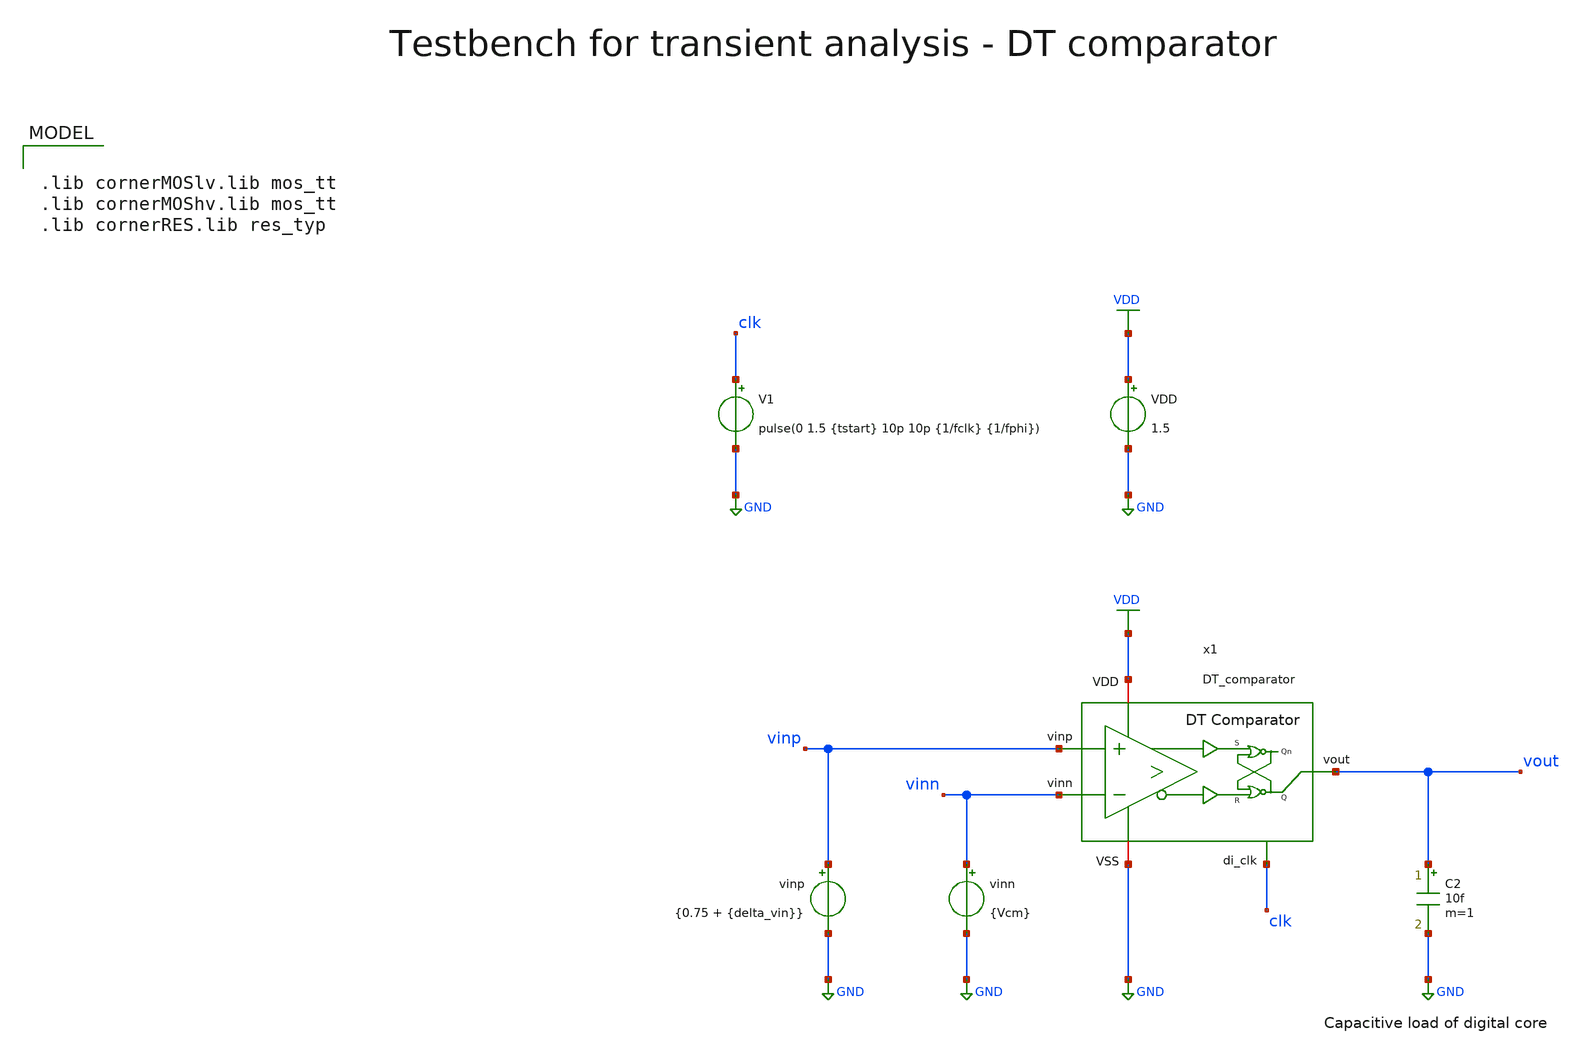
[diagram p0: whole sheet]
** sch_path: SG13G2_ATBS-ADC-main/xschem/comparator/discrete_time/testbenches/DT_comparator_tb_tran.sch
**.subckt DT_comparator_tb_tran
VDD VDD GND 1.5
V1 clk GND pulse(0 1.5 {tstart} 10p 10p {1/fclk} {1/fphi})
vinn vinn GND {Vcm}
vinp vinp GND {0.75 + {delta_vin}}
C2 vout GND 10f m=1
x1 VDD vinp vout vinn clk GND DT_comparator
**** begin user architecture code

.lib cornerMOSlv.lib mos_tt
.lib cornerMOShv.lib mos_tt
.lib cornerRES.lib res_typ



.param temp=27
.param fclk=8000000
.param fphi=62500
.param tstart=2n
.param delta_vin = 10m
.param Vcm=0.75
.csparam fclk=fclk
.csparam tstart=tstart
.options savecurrents reltol=1e-3 abstol=1e-12 gmin=1e-15
.ic v(vout) = 0
.control
save all

* Operating Point Analysis
op
remzerovec
write DT_comparator_tb_tran.raw
set appendwrite

* Transient Analysis
* tran 4p 20n
tran 40p 150n
write DT_comparator_tb_tran.raw

* Measure vcpp_min & vcpn_min
let tmeas = 1/fclk
meas tran vcpp_min FIND v(x1.x1.vcpp) at=tmeas
meas tran vcpn_min FIND v(x1.x1.vcpn) at=tmeas

* Measure Propagation Delay
* Time from clock rising edge to 90% VDD of vout
let vout_limit = 0.9 * 1.5
meas tran tcross WHEN v(vout)=vout_limit CROSS=1
let tpd = tcross - tstart
echo Propagation Delay $&tpd s

* Calculate Energy / Conversion
* i_int in As
* energy_conv in Ws = J
let N = 1
let t_conv = 150n
meas tran i_int INTEG i(VDD) from=tstart to=t_conv
let energy_conv = 1.5 * i_int / N

let energy_conv_femto = energy_conv * 1e15
echo Energy / Conversion $&energy_conv_femto fJ/conv

* Plotting
plot v(clk) v(vinp) v(vinn) v(x1.x1.vs) v(x1.x1.vcpp) v(x1.x1.vcpn) v(x1.voutp_comp)
+ v(x1.voutn_comp) v(vout)
plot i(VDD)

* Writing Data
set wr_singlescale
set wr_vecnames
let vs=x1.x1.vs
let vcpp=x1.x1.vcpp
let vcpn=x1.x1.vcpn
let voutp_comp=x1.voutp_comp
let voutn_comp=x1.voutn_comp
wrdata /foss/designs/SG13G2_ATBS-ADC-main/python/plot_simulations/data/DT_comparator_tb_tran.txt
+ v(clk) v(vinp) v(vinn) v(vs) v(vcpp) v(vcpn) v(voutp_comp) v(voutn_comp) v(vout)

*quit
.endc

**** end user architecture code
**.ends

* expanding   symbol:  comparator/discrete_time/DT_comparator.sym # of pins=6
** sym_path: SG13G2_ATBS-ADC-main/xschem/comparator/discrete_time/DT_comparator.sym
** sch_path: SG13G2_ATBS-ADC-main/xschem/comparator/discrete_time/DT_comparator.sch
.subckt DT_comparator VDD vinp vout vinn di_clk VSS
*.iopin VDD
*.opin vout
*.iopin VSS
*.ipin vinp
*.ipin vinn
*.ipin di_clk
x2 VDD voutp_comp voutp_buf VSS buffer_lv W_P_INV=1.0u L_P_INV=0.13u W_N_INV=1.0u L_N_INV=0.13u
x3 VDD voutn_comp voutn_buf VSS buffer_lv W_P_INV=1.0u L_P_INV=0.13u W_N_INV=1.0u L_N_INV=0.13u
x5 VDD di_clk net1 VSS inverter_lv W_P=1.0u L_P=0.13u W_N=1.0u L_N=0.13u
* noconn #net2
x4 VDD voutp_buf net2 VSS vout voutn_buf SR_latch W_P_SR=1.0u L_P_SR=0.13u W_N_SR=1.0u L_N_SR=0.13u
x1 net1 di_clk VDD voutp_comp vinp VSS voutn_comp vinn dynamic_biasing_comparator
.ends


* expanding   symbol:  buffer/buffer_lv.sym # of pins=4
** sym_path: SG13G2_ATBS-ADC-main/xschem/buffer/buffer_lv.sym
** sch_path: SG13G2_ATBS-ADC-main/xschem/buffer/buffer_lv.sch
.subckt buffer_lv VDD vin vout VSS  W_P_INV=3.0u L_P_INV=0.13u W_N_INV=1.0u L_N_INV=0.13u
*.ipin vin
*.iopin VDD
*.iopin VSS
*.opin vout
x1 VDD vin net1 VSS inverter_lv W_P=W_P_INV L_P=L_P_INV W_N=W_N_INV L_N=L_N_INV
x2 VDD net1 vout VSS inverter_lv W_P=W_P_INV L_P=L_P_INV W_N=W_N_INV L_N=L_N_INV
.ends


* expanding   symbol:  inverter/inverter_lv.sym # of pins=4
** sym_path: SG13G2_ATBS-ADC-main/xschem/inverter/inverter_lv.sym
** sch_path: SG13G2_ATBS-ADC-main/xschem/inverter/inverter_lv.sch
.subckt inverter_lv VDD vin vout VSS  W_P=3.0u L_P=0.13u W_N=1.0u L_N=0.13u
*.ipin vin
*.iopin VDD
*.iopin VSS
*.opin vout
XM1 vout vin VDD VDD sg13_lv_pmos w=W_P l=L_P ng=1 m=1 mm_ok=1
XM2 vout vin VSS VSS sg13_lv_nmos w=W_N l=L_N ng=1 m=1 mm_ok=1
.ends


* expanding   symbol:  comparator/SR_latch/SR_latch.sym # of pins=6
** sym_path: SG13G2_ATBS-ADC-main/xschem/comparator/SR_latch/SR_latch.sym
** sch_path: SG13G2_ATBS-ADC-main/xschem/comparator/SR_latch/SR_latch.sch
.subckt SR_latch VDD S Qn VSS Q R  W_P_SR=1.0u L_P_SR=0.13u W_N_SR=1.0u L_N_SR=0.13u
*.iopin VDD
*.opin Q
*.iopin VSS
*.ipin S
*.ipin R
*.opin Qn
x1 VDD Q R Qn VSS NOR_gate W_P=W_P_SR L_P=L_P_SR W_N=W_N_SR L_N=L_N_SR
x2 VDD Qn Q S VSS NOR_gate W_P=W_P_SR L_P=L_P_SR W_N=W_N_SR L_N=L_N_SR
.ends


* expanding   symbol:  comparator/discrete_time/Dynamic-biasing/dynamic_biasing_comparator.sym # of
*+ pins=8
** sym_path: SG13G2_ATBS-ADC-main/xschem/comparator/discrete_time/Dynamic-biasing/dynamic_biasing_comparator.sym
** sch_path: SG13G2_ATBS-ADC-main/xschem/comparator/discrete_time/Dynamic-biasing/dynamic_biasing_comparator.sch
.subckt dynamic_biasing_comparator di_clk_n di_clk VDD voutp vinp VSS voutn vinn
*.iopin VDD
*.opin voutp
*.opin voutn
*.ipin di_clk_n
*.iopin VSS
*.ipin vinp
*.ipin vinn
*.ipin di_clk
XM3a vs di_clk vctail VSS sg13_lv_nmos w=1.0u l=0.13u ng=1 m=1 mm_ok=1
XM12 voutp di_clk_n VSS VSS sg13_lv_nmos w=1.0u l=0.13u ng=1 m=1 mm_ok=1
XM8 net1 voutn VDD VDD sg13_lv_pmos w=2.0u l=0.13u ng=2 m=1 mm_ok=1
XM10 voutp voutn VSS VSS sg13_lv_nmos w=1.0u l=0.13u ng=1 m=1 mm_ok=1
XM11 voutn voutp VSS VSS sg13_lv_nmos w=1.0u l=0.13u ng=1 m=1 mm_ok=1
XM13 voutn di_clk_n VSS VSS sg13_lv_nmos w=1.0u l=0.13u ng=1 m=1 mm_ok=1
CPn vcpn VSS 300f m=1
CPp vcpp VSS 300f m=1
XM9 net2 voutp VDD VDD sg13_lv_pmos w=2.0u l=0.13u ng=2 m=1 mm_ok=1
XM6 voutp vcpn net1 VDD sg13_lv_pmos w=2.0u l=0.13u ng=2 m=1 mm_ok=1
XM7 voutn vcpp net2 VDD sg13_lv_pmos w=2.0u l=0.13u ng=2 m=1 mm_ok=1
CTAIL vctail VSS 600f m=1
XM3b vctail di_clk_n VSS VSS sg13_lv_nmos w=1.0u l=0.13u ng=1 m=1 mm_ok=1
XM1 vcpn vinp vs VSS sg13_lv_nmos w=1.0u l=0.13u ng=1 m=1 mm_ok=1
XM2 vcpp vinn vs VSS sg13_lv_nmos w=1.0u l=0.13u ng=1 m=1 mm_ok=1
XM4 vcpn di_clk VDD VDD sg13_lv_pmos w=1.0u l=0.13u ng=1 m=1 mm_ok=1
XM5 vcpp di_clk VDD VDD sg13_lv_pmos w=1.0u l=0.13u ng=1 m=1 mm_ok=1
.ends


* expanding   symbol:  comparator/NOR_gate/NOR_gate.sym # of pins=5
** sym_path: SG13G2_ATBS-ADC-main/xschem/comparator/NOR_gate/NOR_gate.sym
** sch_path: SG13G2_ATBS-ADC-main/xschem/comparator/NOR_gate/NOR_gate.sch
.subckt NOR_gate VDD C A B VSS  W_P=1.0u L_P=0.13u W_N=0.5u L_N=0.13u
*.iopin VDD
*.opin C
*.iopin VSS
*.ipin A
*.ipin B
XM1 C A VSS VSS sg13_lv_nmos w=W_N l=L_N ng=1 m=1 mm_ok=1
XM2 C B VSS VSS sg13_lv_nmos w=W_N l=L_N ng=1 m=1 mm_ok=1
XM3 C B net1 VDD sg13_lv_pmos w=W_P l=L_P ng=1 m=1 mm_ok=1
XM4 net1 A VDD VDD sg13_lv_pmos w=W_P l=L_P ng=1 m=1 mm_ok=1
XM5 C A net2 VDD sg13_lv_pmos w=W_P l=L_P ng=1 m=1 mm_ok=1
XM6 net2 B VDD VDD sg13_lv_pmos w=W_P l=L_P ng=1 m=1 mm_ok=1
.ends

.GLOBAL GND
.GLOBAL VDD
.end
